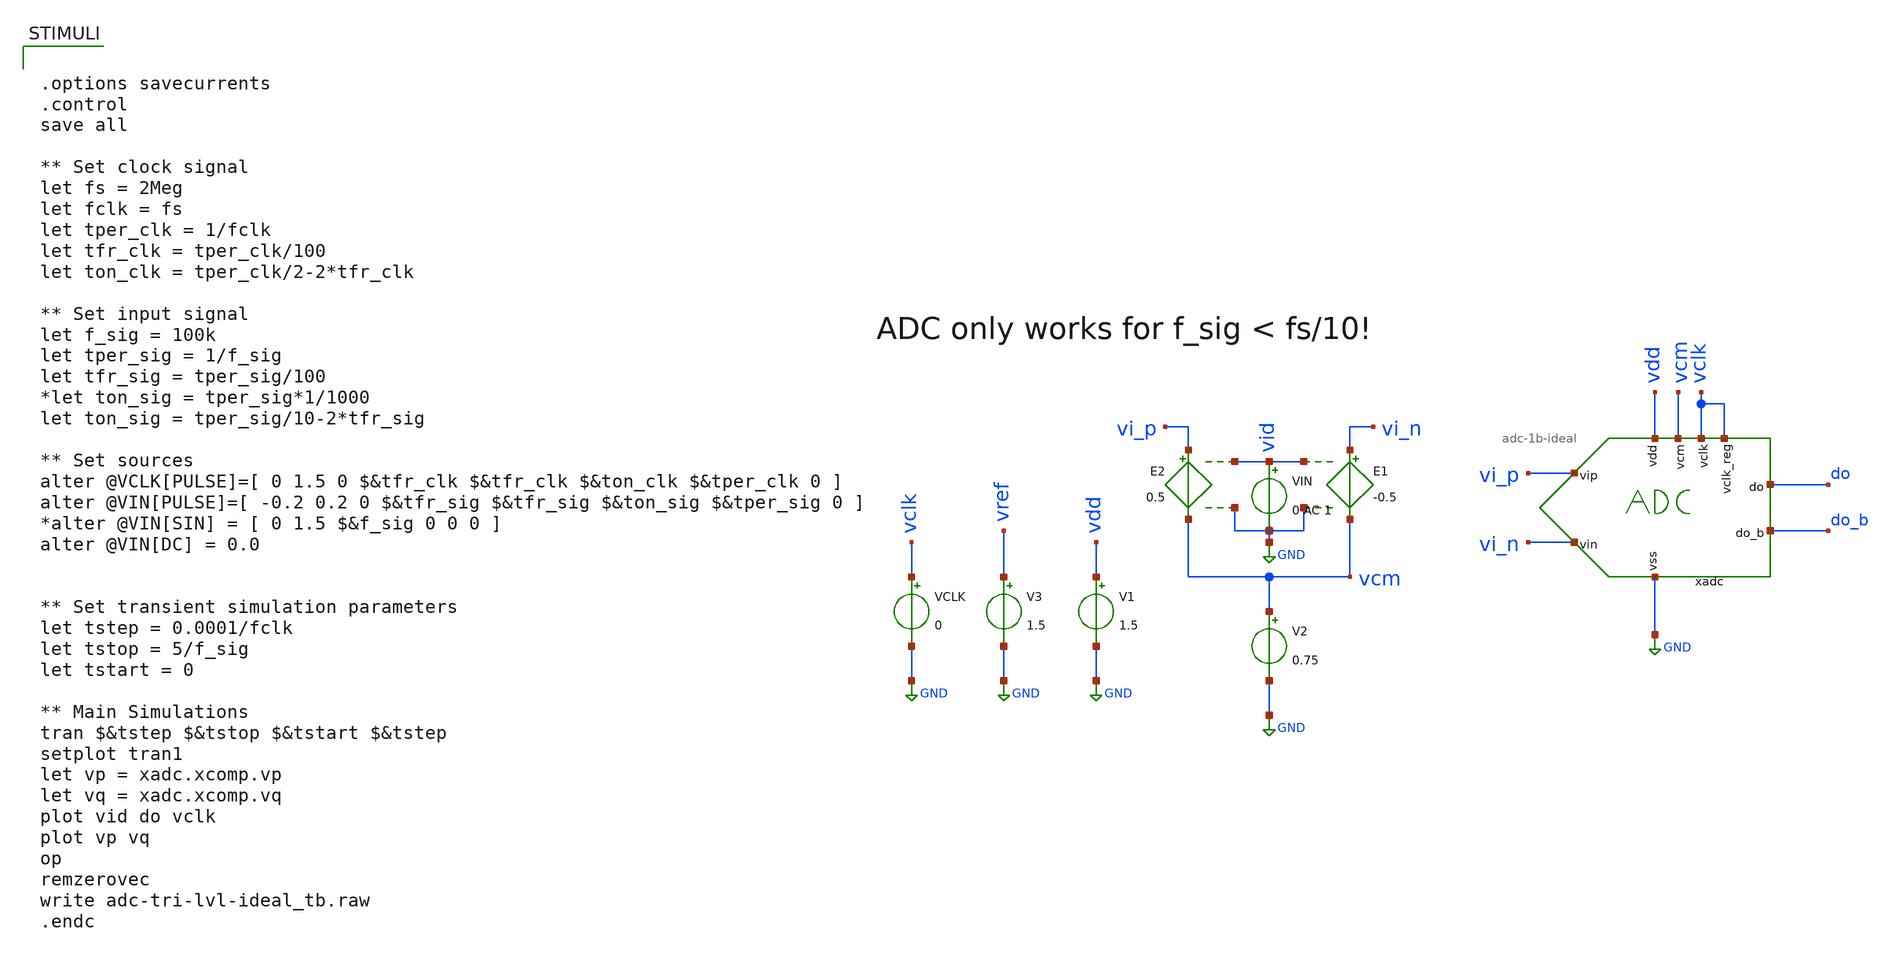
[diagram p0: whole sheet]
** sch_path: xschem/adc-1b-ideal_tb.sch
**.subckt adc-1b-ideal_tb
V2 vcm GND 0.75
E1 vi_n vcm vid GND -0.5
E2 vi_p vcm vid GND 0.5
VIN vid GND 0 AC 1
VCLK vclk GND 0
V3 vref GND 1.5
xadc do vi_p vi_n vcm vclk GND do_b vdd vclk adc-1b-ideal
V1 vdd GND 1.5
**** begin user architecture code


.options savecurrents
.control
save all

** Set clock signal
let fs = 2Meg
let fclk = fs
let tper_clk = 1/fclk
let tfr_clk = tper_clk/100
let ton_clk = tper_clk/2-2*tfr_clk

** Set input signal
let f_sig = 100k
let tper_sig = 1/f_sig
let tfr_sig = tper_sig/100
*let ton_sig = tper_sig*1/1000
let ton_sig = tper_sig/10-2*tfr_sig

** Set sources
alter @VCLK[PULSE]=[ 0 1.5 0 $&tfr_clk $&tfr_clk $&ton_clk $&tper_clk 0 ]
alter @VIN[PULSE]=[ -0.2 0.2 0 $&tfr_sig $&tfr_sig $&ton_sig $&tper_sig 0 ]
*alter @VIN[SIN] = [ 0 1.5 $&f_sig 0 0 0 ]
alter @VIN[DC] = 0.0


** Set transient simulation parameters
let tstep = 0.0001/fclk
let tstop = 5/f_sig
let tstart = 0

** Main Simulations
tran $&tstep $&tstop $&tstart $&tstep
setplot tran1
let vp = xadc.xcomp.vp
let vq = xadc.xcomp.vq
plot vid do vclk
plot vp vq
op
remzerovec
write adc-tri-lvl-ideal_tb.raw
.endc

**** end user architecture code
**.ends

* expanding   symbol:  adc-1b-ideal.sym # of pins=9
** sym_path: xschem/legacy/adc-1b-ideal.sym
** sch_path: xschem/legacy/adc-1b-ideal.sch
.subckt adc-1b-ideal do vip vin vcm vclk vss do_b vdd vclk_reg
*.iopin vss
*.ipin vip
*.ipin vin
*.ipin vcm
*.ipin vclk
*.opin do_b
*.opin do
*.iopin vdd
*.ipin vclk_reg
**** begin user architecture code


.model adc_buf adc_bridge(in_low=0.7499 in_high=0.7501)
.model dac1 dac_bridge(out_low = 0 out_high = 1.5 out_undef = 0 input_load = 0.1e-15 t_rise =
+ 0.01e-9 t_fall = 0.01e-9)
.model nor1 d_nor(rise_delay = 0.01e-9 fall_delay = 0.01e-9 input_load = 0.01e-15)
.model dlatch1 d_dlatch(data_delay = 0.01e-9 enable_delay = 0.01e-9 set_delay = 0.01e-9 reset_delay
+ = 0.01e-9 ic = 0 rise_delay = 0.01e-9 fall_delay = 0.01e-9)
.model dff1 d_dff(clk_delay = 0.01e-9 set_delay = 0.01e-9 reset_delay = 0.01e-9 ic = 0 rise_delay =
+ 0.01e-9 fall_delay = 0.01e-9)


**** end user architecture code
A3 [ NQ1 ] [ do_b ] dac1
A2 [ Q1 ] [ do ] dac1
**** begin user architecture code


a21 [D0 NQ0] Q0 nor1
a22 [ND0 Q0] NQ0 nor1


**** end user architecture code
xcomp vdd vclk ND0 D0 vin vcm vcm vip vss sal-macro
**** begin user architecture code


a23 Q0 CLK NULL NULL %d(Q_REG0 NULL) dlatch1
a24 NQ0 CLK NULL NULL %d(NQ_REG0 NULL) dlatch1


**** end user architecture code
A1 [ vclk ] [ CLK ] adc_buf
**** begin user architecture code


a31 Q_REG0 CLK_REG NULL NULL %d(Q1 NULL) dff1
a32 NQ_REG0 CLK_REG NULL NULL %d(NQ1 NULL) dff1


**** end user architecture code
A4 [ vclk_reg ] [ CLK_REG ] adc_buf
.ends


* expanding   symbol:  sal-macro.sym # of pins=9
** sym_path: xschem/sal-macro.sym
** sch_path: xschem/sal-macro.sch
.subckt sal-macro vdd vclk do_b do vin_1 vip_2 vin_2 vip_1 vss
*.iopin vss
*.ipin vip_1
*.ipin vip_2
*.ipin vin_2
*.opin do
*.ipin vin_1
*.iopin vdd
*.opin do_b
*.ipin vclk
A1 [ net5 ] [ do ] comp0
G1 net2 net1 vip_1 net1 10e-6
**** begin user architecture code

.model comp0 adc_bridge(in_low=0.74 in_high=0.76)

**** end user architecture code
G3 net3 net1 vin_1 net1 10e-6
S1 net1 vss vclk vss SW1
G2 net5 net3 net4 net3 10e-6
G4 net4 net2 net5 net2 10e-6
G5 vdd net5 vdd net4 10e-6
G6 vdd net4 vdd net5 10e-6
S3 vdd net4 vdd vclk SW1
S4 vdd net2 vdd vclk SW1
S5 vdd net5 vdd vclk SW1
S6 vdd net2 vdd vclk SW1
A2 [ net4 ] [ do_b ] comp0
R1 vdd net4 1Meg m=1
R2 vdd net5 1Meg m=1
R3 net5 net3 1Meg m=1
R4 net4 net2 1Meg m=1
R5 net2 net1 100Meg m=1
R6 net3 net1 100e-6 m=1
.ends

.GLOBAL GND
**** begin user architecture code
.MODEL SW1 SW( VT=0.75 VH=0.01 RON=1 ROFF=100Meg )
**** end user architecture code
.end
